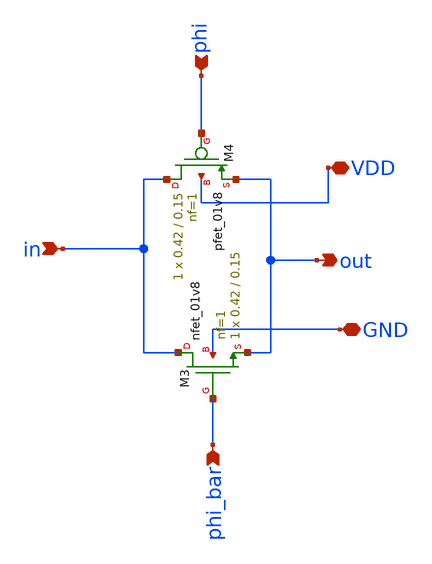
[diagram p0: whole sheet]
** sch_path: assignments/assignment6/transmission_gate.sch
**.subckt transmission_gate in out phi phi_bar GND VDD
*.ipin in
*.opin out
*.ipin phi
*.ipin phi_bar
*.iopin GND
*.iopin VDD
XM3 in phi_bar out GND sky130_fd_pr__nfet_01v8 L=0.15 W=0.42 nf=1 ad='int((nf+1)/2) * W/nf * 0.29' as='int((nf+2)/2) * W/nf * 0.29'
+ pd='2*int((nf+1)/2) * (W/nf + 0.29)' ps='2*int((nf+2)/2) * (W/nf + 0.29)' nrd='0.29 / W' nrs='0.29 / W'
+ sa=0 sb=0 sd=0 mult=1 m=1
XM4 in phi out VDD sky130_fd_pr__pfet_01v8 L=0.15 W=0.42 nf=1 ad='int((nf+1)/2) * W/nf * 0.29' as='int((nf+2)/2) * W/nf * 0.29'
+ pd='2*int((nf+1)/2) * (W/nf + 0.29)' ps='2*int((nf+2)/2) * (W/nf + 0.29)' nrd='0.29 / W' nrs='0.29 / W'
+ sa=0 sb=0 sd=0 mult=1 m=1
**.ends
.end
